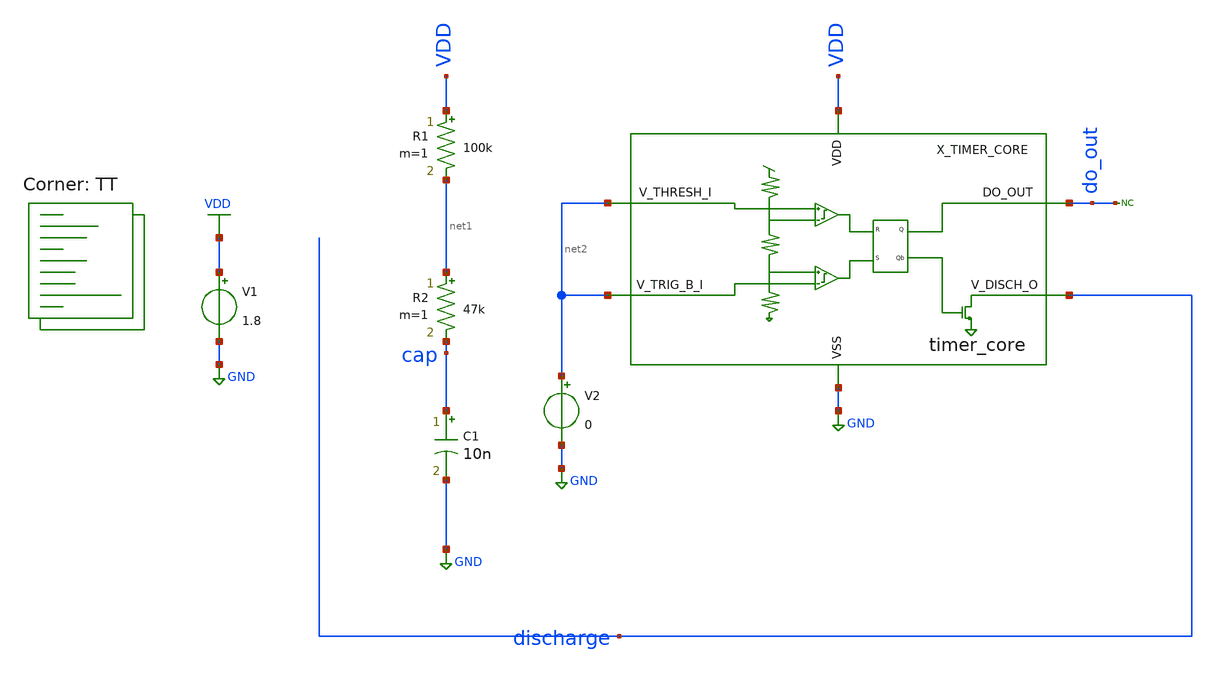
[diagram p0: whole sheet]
** sch_path: xsch/tb/timer_core/tb_timer_core_astable.sch
**.subckt tb_timer_core_astable
V1 VDD GND 1.8
R1 VDD net1 100k m=1
R2 net1 cap 47k m=1
C1 cap GND 10n m=1
* noconn do_out
X_TIMER_CORE net2 net2 do_out discharge VDD GND timer_core
V2 net2 GND 0
**** begin user architecture code


.ic v(cap) = 0

.control
	tran 0.1m 100m
	;plot v(cap) v(discharge) v(do_out)

	;plot v(x_timer_core.v0p6) v(x_timer_core.v1p2) v(x_timer_core.bias_p) v(x_timer_core.bias_1)
+ v(x_timer_core.bias_2) v(x_timer_core.bias_3) v(x_timer_core.bias_n)

	;plot v(x_timer_core.sr_r) v(x_timer_core.sr_s) v(x_timer_core.v1p2) v(x_timer_core.v0p6)
	;plot v(x_timer_core.bias_n) v(x_timer_core.bias_1) v(x_timer_core.bias_2) v(x_timer_core.bias_3)
+ v(x_timer_core.bias_p)
	plot v(x_timer_core.sr_r) v(x_timer_core.sr_s) v(x_timer_core.v1p2)
plot v(x_timer_core.x_comp_p_top.latch_left) v(x_timer_core.x_comp_p_top.latch_right)
+ v(x_timer_core.x_comp_p_top.tail) v(x_timer_core.x_comp_p_top.out_left)
.endc
.end


.lib $::SKYWATER_MODELS/sky130.lib.spice TT


.save all

.savecurrents


**** end user architecture code
**.ends
.GLOBAL VDD
.GLOBAL GND
.end
